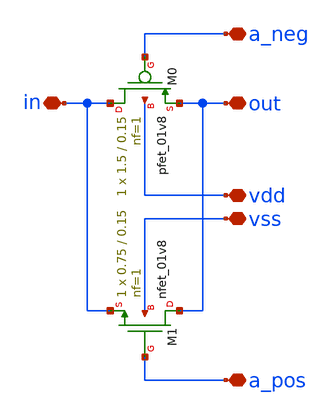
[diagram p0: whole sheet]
** sch_path: design/blocks/transmissiongate/schematic/transmissiongate.sch
**.subckt transmissiongate vdd vss out in a_neg a_pos
*.iopin vdd
*.iopin vss
*.iopin out
*.iopin in
*.iopin a_neg
*.iopin a_pos
XM0 in a_neg out vdd sky130_fd_pr__pfet_01v8 L=0.15 W=1.5 nf=1 ad='int((nf+1)/2) * W/nf * 0.29' as='int((nf+2)/2) * W/nf * 0.29'
+ pd='2*int((nf+1)/2) * (W/nf + 0.29)' ps='2*int((nf+2)/2) * (W/nf + 0.29)' nrd='0.29 / W' nrs='0.29 / W'
+ sa=0 sb=0 sd=0 mult=1 m=1
XM1 out a_pos in vss sky130_fd_pr__nfet_01v8 L=0.15 W=0.75 nf=1 ad='int((nf+1)/2) * W/nf * 0.29' as='int((nf+2)/2) * W/nf * 0.29'
+ pd='2*int((nf+1)/2) * (W/nf + 0.29)' ps='2*int((nf+2)/2) * (W/nf + 0.29)' nrd='0.29 / W' nrs='0.29 / W'
+ sa=0 sb=0 sd=0 mult=1 m=1
**.ends
.end
